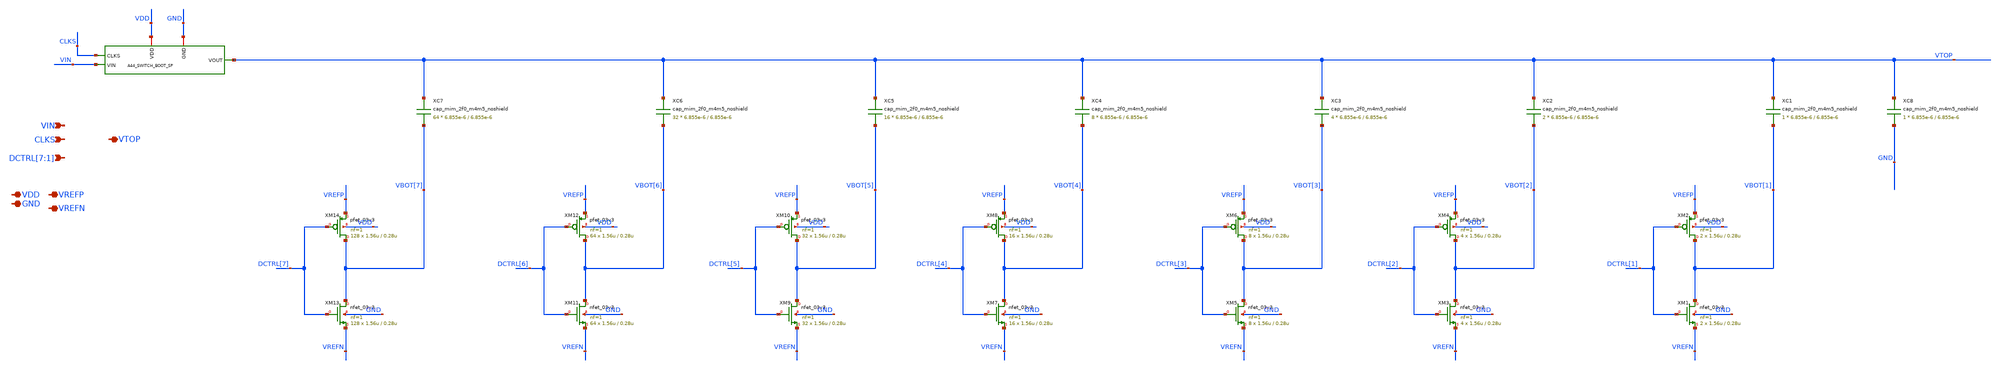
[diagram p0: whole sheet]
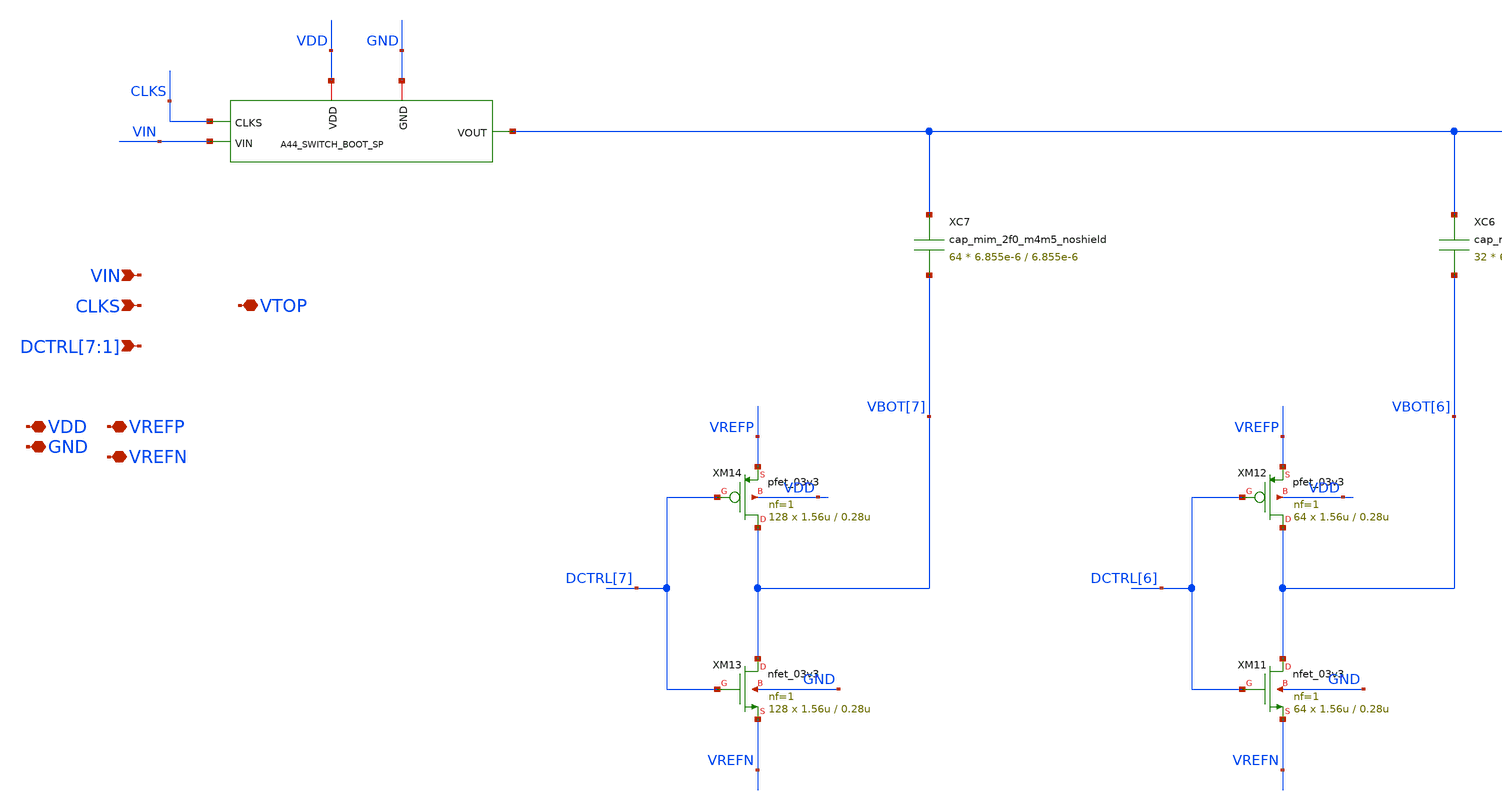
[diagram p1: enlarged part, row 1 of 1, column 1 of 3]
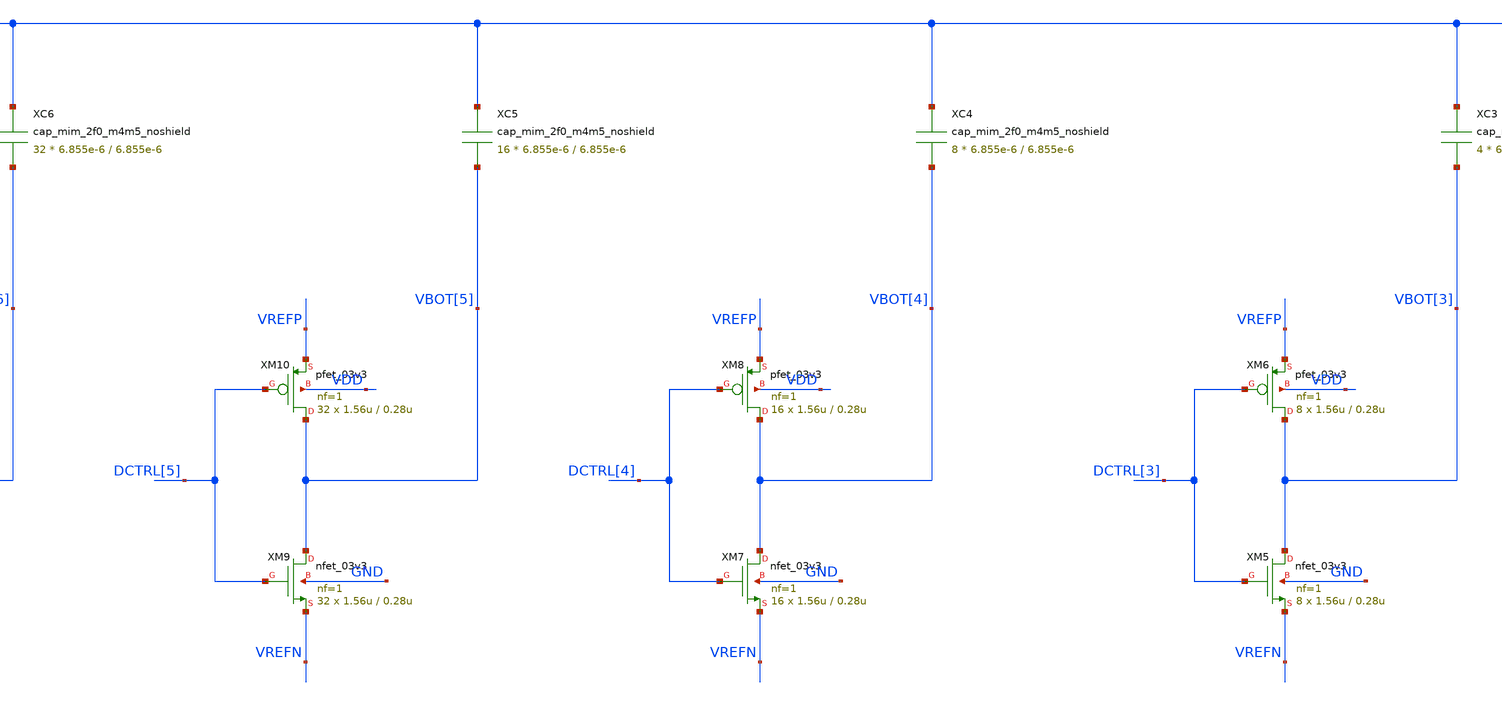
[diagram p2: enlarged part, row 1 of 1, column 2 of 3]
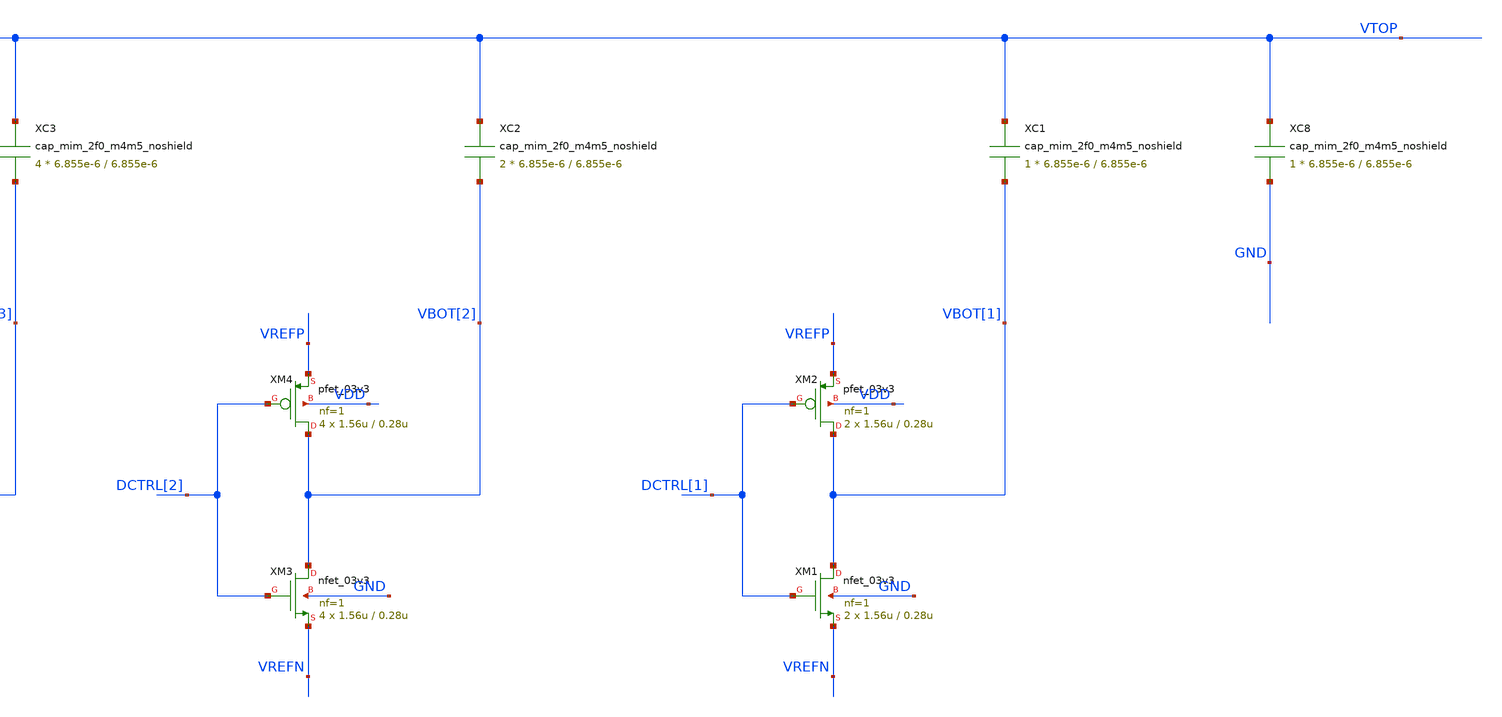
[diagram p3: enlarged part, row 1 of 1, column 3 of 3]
** sch_path: verification/a44_r2/01_CURRENT_CIRCUIT_FILES/xschem/CDAC.sch
**.subckt CDAC VIN CLKS VDD GND VREFP VREFN VTOP
*+ DCTRL[7],DCTRL[6],DCTRL[5],DCTRL[4],DCTRL[3],DCTRL[2],DCTRL[1]
*.ipin VIN
*.ipin CLKS
*.iopin VDD
*.iopin GND
*.iopin VREFP
*.iopin VREFN
*.iopin VTOP
*.ipin DCTRL[7],DCTRL[6],DCTRL[5],DCTRL[4],DCTRL[3],DCTRL[2],DCTRL[1]
XM1 VBOT[1] DCTRL[1] VREFN GND nfet_03v3 L=0.28u W=1.56u nf=1 ad='int((nf+1)/2) * W/nf * 0.18u' as='int((nf+2)/2) * W/nf * 0.18u'
+ pd='2*int((nf+1)/2) * (W/nf + 0.18u)' ps='2*int((nf+2)/2) * (W/nf + 0.18u)' nrd='0.18u / W' nrs='0.18u / W'
+ sa=0 sb=0 sd=0 m=2
XM2 VBOT[1] DCTRL[1] VREFP VDD pfet_03v3 L=0.28u W=1.56u nf=1 ad='int((nf+1)/2) * W/nf * 0.18u' as='int((nf+2)/2) * W/nf * 0.18u'
+ pd='2*int((nf+1)/2) * (W/nf + 0.18u)' ps='2*int((nf+2)/2) * (W/nf + 0.18u)' nrd='0.18u / W' nrs='0.18u / W'
+ sa=0 sb=0 sd=0 m=2
XC1 VTOP VBOT[1] cap_mim_2f0_m4m5_noshield c_width=6.855e-6 c_length=6.855e-6 m=1
XM3 VBOT[2] DCTRL[2] VREFN GND nfet_03v3 L=0.28u W=1.56u nf=1 ad='int((nf+1)/2) * W/nf * 0.18u' as='int((nf+2)/2) * W/nf * 0.18u'
+ pd='2*int((nf+1)/2) * (W/nf + 0.18u)' ps='2*int((nf+2)/2) * (W/nf + 0.18u)' nrd='0.18u / W' nrs='0.18u / W'
+ sa=0 sb=0 sd=0 m=4
XM4 VBOT[2] DCTRL[2] VREFP VDD pfet_03v3 L=0.28u W=1.56u nf=1 ad='int((nf+1)/2) * W/nf * 0.18u' as='int((nf+2)/2) * W/nf * 0.18u'
+ pd='2*int((nf+1)/2) * (W/nf + 0.18u)' ps='2*int((nf+2)/2) * (W/nf + 0.18u)' nrd='0.18u / W' nrs='0.18u / W'
+ sa=0 sb=0 sd=0 m=4
XC2 VTOP VBOT[2] cap_mim_2f0_m4m5_noshield c_width=6.855e-6 c_length=6.855e-6 m=2
XM5 VBOT[3] DCTRL[3] VREFN GND nfet_03v3 L=0.28u W=1.56u nf=1 ad='int((nf+1)/2) * W/nf * 0.18u' as='int((nf+2)/2) * W/nf * 0.18u'
+ pd='2*int((nf+1)/2) * (W/nf + 0.18u)' ps='2*int((nf+2)/2) * (W/nf + 0.18u)' nrd='0.18u / W' nrs='0.18u / W'
+ sa=0 sb=0 sd=0 m=8
XM6 VBOT[3] DCTRL[3] VREFP VDD pfet_03v3 L=0.28u W=1.56u nf=1 ad='int((nf+1)/2) * W/nf * 0.18u' as='int((nf+2)/2) * W/nf * 0.18u'
+ pd='2*int((nf+1)/2) * (W/nf + 0.18u)' ps='2*int((nf+2)/2) * (W/nf + 0.18u)' nrd='0.18u / W' nrs='0.18u / W'
+ sa=0 sb=0 sd=0 m=8
XC3 VTOP VBOT[3] cap_mim_2f0_m4m5_noshield c_width=6.855e-6 c_length=6.855e-6 m=4
XM7 VBOT[4] DCTRL[4] VREFN GND nfet_03v3 L=0.28u W=1.56u nf=1 ad='int((nf+1)/2) * W/nf * 0.18u' as='int((nf+2)/2) * W/nf * 0.18u'
+ pd='2*int((nf+1)/2) * (W/nf + 0.18u)' ps='2*int((nf+2)/2) * (W/nf + 0.18u)' nrd='0.18u / W' nrs='0.18u / W'
+ sa=0 sb=0 sd=0 m=16
XM8 VBOT[4] DCTRL[4] VREFP VDD pfet_03v3 L=0.28u W=1.56u nf=1 ad='int((nf+1)/2) * W/nf * 0.18u' as='int((nf+2)/2) * W/nf * 0.18u'
+ pd='2*int((nf+1)/2) * (W/nf + 0.18u)' ps='2*int((nf+2)/2) * (W/nf + 0.18u)' nrd='0.18u / W' nrs='0.18u / W'
+ sa=0 sb=0 sd=0 m=16
XC4 VTOP VBOT[4] cap_mim_2f0_m4m5_noshield c_width=6.855e-6 c_length=6.855e-6 m=8
XM9 VBOT[5] DCTRL[5] VREFN GND nfet_03v3 L=0.28u W=1.56u nf=1 ad='int((nf+1)/2) * W/nf * 0.18u' as='int((nf+2)/2) * W/nf * 0.18u'
+ pd='2*int((nf+1)/2) * (W/nf + 0.18u)' ps='2*int((nf+2)/2) * (W/nf + 0.18u)' nrd='0.18u / W' nrs='0.18u / W'
+ sa=0 sb=0 sd=0 m=32
XM10 VBOT[5] DCTRL[5] VREFP VDD pfet_03v3 L=0.28u W=1.56u nf=1 ad='int((nf+1)/2) * W/nf * 0.18u' as='int((nf+2)/2) * W/nf * 0.18u'
+ pd='2*int((nf+1)/2) * (W/nf + 0.18u)' ps='2*int((nf+2)/2) * (W/nf + 0.18u)' nrd='0.18u / W' nrs='0.18u / W'
+ sa=0 sb=0 sd=0 m=32
XC5 VTOP VBOT[5] cap_mim_2f0_m4m5_noshield c_width=6.855e-6 c_length=6.855e-6 m=16
XM11 VBOT[6] DCTRL[6] VREFN GND nfet_03v3 L=0.28u W=1.56u nf=1 ad='int((nf+1)/2) * W/nf * 0.18u' as='int((nf+2)/2) * W/nf * 0.18u'
+ pd='2*int((nf+1)/2) * (W/nf + 0.18u)' ps='2*int((nf+2)/2) * (W/nf + 0.18u)' nrd='0.18u / W' nrs='0.18u / W'
+ sa=0 sb=0 sd=0 m=64
XM12 VBOT[6] DCTRL[6] VREFP VDD pfet_03v3 L=0.28u W=1.56u nf=1 ad='int((nf+1)/2) * W/nf * 0.18u' as='int((nf+2)/2) * W/nf * 0.18u'
+ pd='2*int((nf+1)/2) * (W/nf + 0.18u)' ps='2*int((nf+2)/2) * (W/nf + 0.18u)' nrd='0.18u / W' nrs='0.18u / W'
+ sa=0 sb=0 sd=0 m=64
XC6 VTOP VBOT[6] cap_mim_2f0_m4m5_noshield c_width=6.855e-6 c_length=6.855e-6 m=32
XM13 VBOT[7] DCTRL[7] VREFN GND nfet_03v3 L=0.28u W=1.56u nf=1 ad='int((nf+1)/2) * W/nf * 0.18u' as='int((nf+2)/2) * W/nf * 0.18u'
+ pd='2*int((nf+1)/2) * (W/nf + 0.18u)' ps='2*int((nf+2)/2) * (W/nf + 0.18u)' nrd='0.18u / W' nrs='0.18u / W'
+ sa=0 sb=0 sd=0 m=128
XM14 VBOT[7] DCTRL[7] VREFP VDD pfet_03v3 L=0.28u W=1.56u nf=1 ad='int((nf+1)/2) * W/nf * 0.18u' as='int((nf+2)/2) * W/nf * 0.18u'
+ pd='2*int((nf+1)/2) * (W/nf + 0.18u)' ps='2*int((nf+2)/2) * (W/nf + 0.18u)' nrd='0.18u / W' nrs='0.18u / W'
+ sa=0 sb=0 sd=0 m=128
XC7 VTOP VBOT[7] cap_mim_2f0_m4m5_noshield c_width=6.855e-6 c_length=6.855e-6 m=64
XC8 VTOP GND cap_mim_2f0_m4m5_noshield c_width=6.855e-6 c_length=6.855e-6 m=1
x1 CLKS VDD GND VTOP VIN SWITCH_BOOT_SP
**.ends
.end
